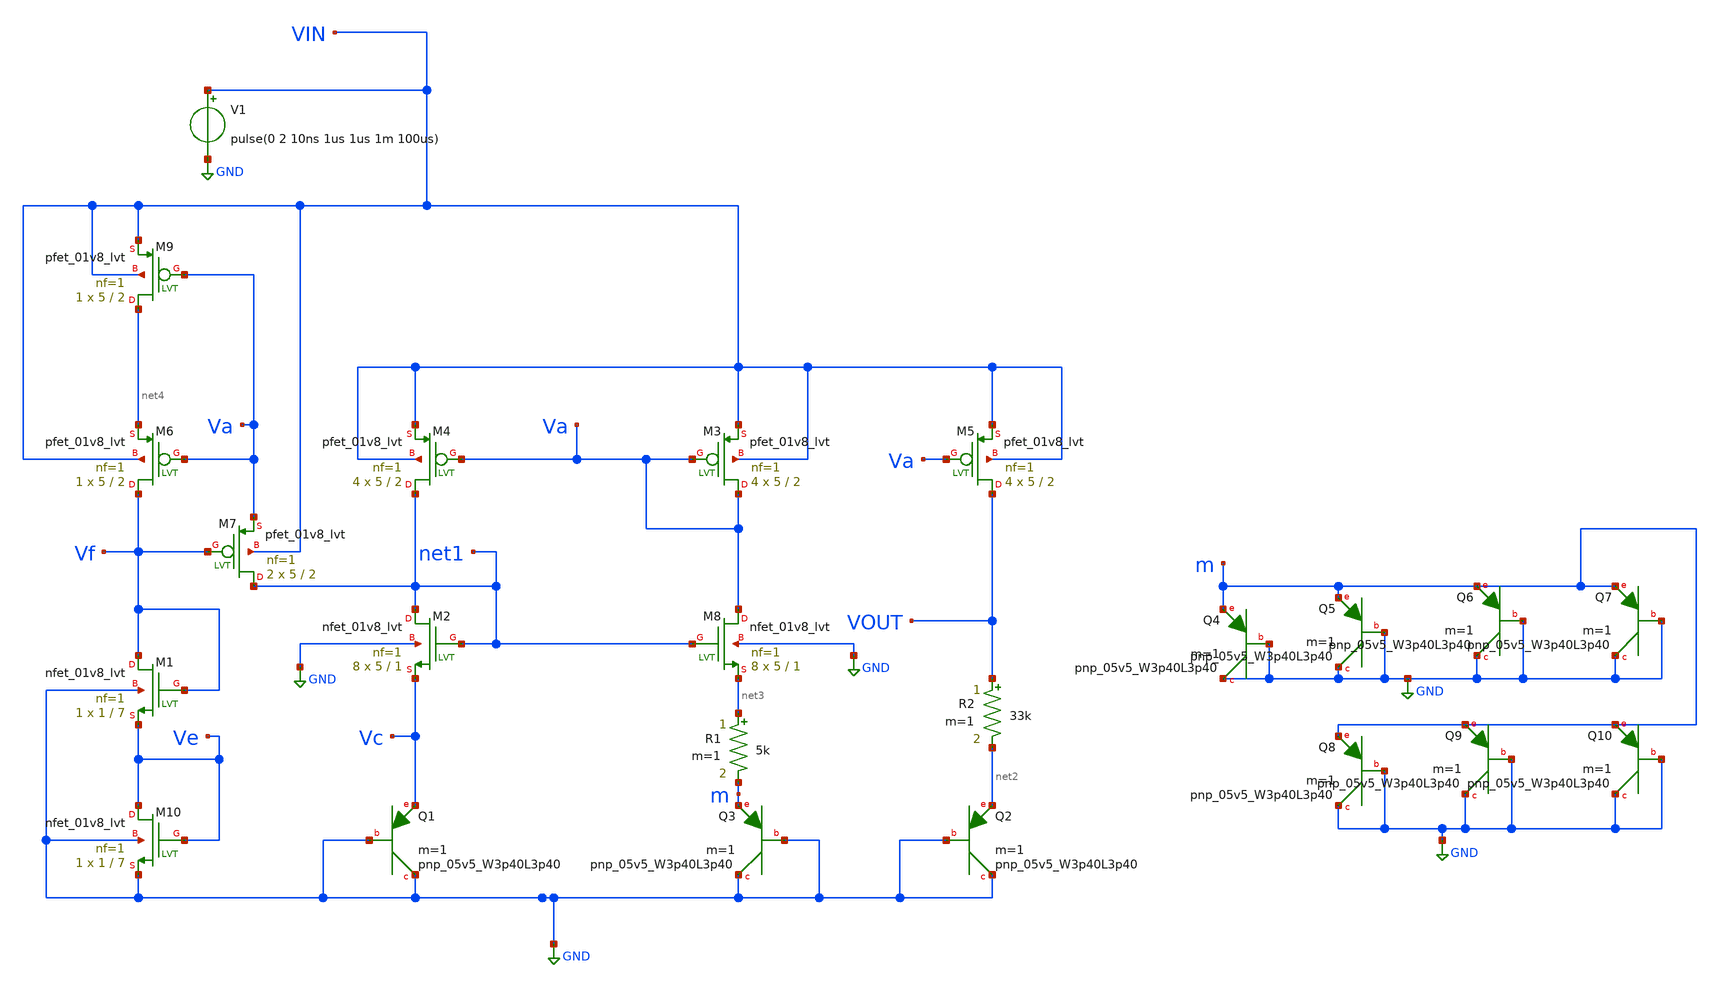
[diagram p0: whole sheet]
** sch_path: Bangap.sch
**.subckt Bangap
XM3 Va Va VIN VIN sky130_fd_pr__pfet_01v8_lvt L=2 W=5 nf=1 ad='int((nf+1)/2) * W/nf * 0.29' as='int((nf+2)/2) * W/nf * 0.29'
+ pd='2*int((nf+1)/2) * (W/nf + 0.29)' ps='2*int((nf+2)/2) * (W/nf + 0.29)' nrd='0.29 / W' nrs='0.29 / W'
+ sa=0 sb=0 sd=0 mult=4 m=4
XM4 net1 Va VIN VIN sky130_fd_pr__pfet_01v8_lvt L=2 W=5 nf=1 ad='int((nf+1)/2) * W/nf * 0.29' as='int((nf+2)/2) * W/nf * 0.29'
+ pd='2*int((nf+1)/2) * (W/nf + 0.29)' ps='2*int((nf+2)/2) * (W/nf + 0.29)' nrd='0.29 / W' nrs='0.29 / W'
+ sa=0 sb=0 sd=0 mult=4 m=4
XM5 VOUT Va VIN VIN sky130_fd_pr__pfet_01v8_lvt L=2 W=5 nf=1 ad='int((nf+1)/2) * W/nf * 0.29' as='int((nf+2)/2) * W/nf * 0.29'
+ pd='2*int((nf+1)/2) * (W/nf + 0.29)' ps='2*int((nf+2)/2) * (W/nf + 0.29)' nrd='0.29 / W' nrs='0.29 / W'
+ sa=0 sb=0 sd=0 mult=4 m=4
XM6 Vf Va net4 VIN sky130_fd_pr__pfet_01v8_lvt L=2 W=5 nf=1 ad='int((nf+1)/2) * W/nf * 0.29' as='int((nf+2)/2) * W/nf * 0.29'
+ pd='2*int((nf+1)/2) * (W/nf + 0.29)' ps='2*int((nf+2)/2) * (W/nf + 0.29)' nrd='0.29 / W' nrs='0.29 / W'
+ sa=0 sb=0 sd=0 mult=1 m=1
XM7 net1 Vf Va VIN sky130_fd_pr__pfet_01v8_lvt L=2 W=5 nf=1 ad='int((nf+1)/2) * W/nf * 0.29' as='int((nf+2)/2) * W/nf * 0.29'
+ pd='2*int((nf+1)/2) * (W/nf + 0.29)' ps='2*int((nf+2)/2) * (W/nf + 0.29)' nrd='0.29 / W' nrs='0.29 / W'
+ sa=0 sb=0 sd=0 mult=2 m=2
XQ1 GND GND Vc sky130_fd_pr__pnp_05v5_W3p40L3p40 m=1
XQ2 GND GND net2 sky130_fd_pr__pnp_05v5_W3p40L3p40 m=1
XQ3 GND GND m sky130_fd_pr__pnp_05v5_W3p40L3p40 m=1
R1 net3 m 5k m=1
R2 VOUT net2 33k m=1
V1 VIN GND pulse(0 2 10ns 1us 1us 1m 100us)
XM9 net4 Va VIN VIN sky130_fd_pr__pfet_01v8_lvt L=2 W=5 nf=1 ad='int((nf+1)/2) * W/nf * 0.29' as='int((nf+2)/2) * W/nf * 0.29'
+ pd='2*int((nf+1)/2) * (W/nf + 0.29)' ps='2*int((nf+2)/2) * (W/nf + 0.29)' nrd='0.29 / W' nrs='0.29 / W'
+ sa=0 sb=0 sd=0 mult=1 m=1
XM1 Vf Vf Ve GND sky130_fd_pr__nfet_01v8_lvt L=7 W=1 nf=1 ad='int((nf+1)/2) * W/nf * 0.29' as='int((nf+2)/2) * W/nf * 0.29'
+ pd='2*int((nf+1)/2) * (W/nf + 0.29)' ps='2*int((nf+2)/2) * (W/nf + 0.29)' nrd='0.29 / W' nrs='0.29 / W'
+ sa=0 sb=0 sd=0 mult=1 m=1
XM2 net1 net1 Vc GND sky130_fd_pr__nfet_01v8_lvt L=1 W=5 nf=1 ad='int((nf+1)/2) * W/nf * 0.29' as='int((nf+2)/2) * W/nf * 0.29'
+ pd='2*int((nf+1)/2) * (W/nf + 0.29)' ps='2*int((nf+2)/2) * (W/nf + 0.29)' nrd='0.29 / W' nrs='0.29 / W'
+ sa=0 sb=0 sd=0 mult=8 m=8
XM8 Va net1 net3 GND sky130_fd_pr__nfet_01v8_lvt L=1 W=5 nf=1 ad='int((nf+1)/2) * W/nf * 0.29' as='int((nf+2)/2) * W/nf * 0.29'
+ pd='2*int((nf+1)/2) * (W/nf + 0.29)' ps='2*int((nf+2)/2) * (W/nf + 0.29)' nrd='0.29 / W' nrs='0.29 / W'
+ sa=0 sb=0 sd=0 mult=8 m=8
XM10 Ve Ve GND GND sky130_fd_pr__nfet_01v8_lvt L=7 W=1 nf=1 ad='int((nf+1)/2) * W/nf * 0.29' as='int((nf+2)/2) * W/nf * 0.29'
+ pd='2*int((nf+1)/2) * (W/nf + 0.29)' ps='2*int((nf+2)/2) * (W/nf + 0.29)' nrd='0.29 / W' nrs='0.29 / W'
+ sa=0 sb=0 sd=0 mult=1 m=1
XQ4 GND GND m sky130_fd_pr__pnp_05v5_W3p40L3p40 m=1
XQ5 GND GND m sky130_fd_pr__pnp_05v5_W3p40L3p40 m=1
XQ6 GND GND m sky130_fd_pr__pnp_05v5_W3p40L3p40 m=1
XQ7 GND GND m sky130_fd_pr__pnp_05v5_W3p40L3p40 m=1
XQ8 GND GND m sky130_fd_pr__pnp_05v5_W3p40L3p40 m=1
XQ9 GND GND m sky130_fd_pr__pnp_05v5_W3p40L3p40 m=1
XQ10 GND GND m sky130_fd_pr__pnp_05v5_W3p40L3p40 m=1
**** begin user architecture code



.options TEMP = 27

* Models
.lib /usr/local/share/pdk/sky130A/libs.tech/ngspice/sky130.lib.spice tt
.iclude /usr/local/share/pdk/sky130A/libs.tech/ngspice/sky130_fd_pr__model__pnp.model.spice

* Data to save
.save all  @M.XM1.msky130_fd_pr__nfet_01v8_lvt[id]  @M.XM1.msky130_fd_pr__nfet_01v8_lvt[value]  @M.XM1.msky130_fd_pr__nfet_01v8_lvt[gm]  @M.XM1.msky130_fd_pr__nfet_01v8_lvt[vth]  @M.XM1.msky130_fd_pr__nfet_01v8_lvt[vds]  @M.XM1.msky130_fd_pr__nfet_01v8_lvt[vdsat]  @M.XM1.msky130_fd_pr__nfet_01v8_lvt[vgs]  @M.XM1.msky130_fd_pr__nfet_01v8_lvt[w]  @M.XM1.msky130_fd_pr__nfet_01v8_lvt[m]  @M.XM2.msky130_fd_pr__nfet_01v8_lvt[id]  @M.XM2.msky130_fd_pr__nfet_01v8_lvt[value]  @M.XM2.msky130_fd_pr__nfet_01v8_lvt[gm]  @M.XM2.msky130_fd_pr__nfet_01v8_lvt[vth]  @M.XM2.msky130_fd_pr__nfet_01v8_lvt[vds]  @M.XM2.msky130_fd_pr__nfet_01v8_lvt[vdsat]  @M.XM2.msky130_fd_pr__nfet_01v8_lvt[vgs]  @M.XM2.msky130_fd_pr__nfet_01v8_lvt[w]  @M.XM2.msky130_fd_pr__nfet_01v8_lvt[m]  @M.XM3.msky130_fd_pr__pfet_01v8_lvt[id]  @M.XM3.msky130_fd_pr__pfet_01v8_lvt[gm]  @M.XM3.msky130_fd_pr__pfet_01v8_lvt[vth]  @M.XM3.msky130_fd_pr__pfet_01v8_lvt[vsd]  @M.XM3.msky130_fd_pr__pfet_01v8_lvt[vdsat]  @M.XM3.msky130_fd_pr__pfet_01v8_lvt[vsg]  @M.XM3.msky130_fd_pr__pfet_01v8_lvt[w]  @M.XM3.msky130_fd_pr__pfet_01v8_lvt[m]  @M.XM4.msky130_fd_pr__pfet_01v8_lvt[id]  @M.XM4.msky130_fd_pr__pfet_01v8_lvt[gm]  @M.XM4.msky130_fd_pr__pfet_01v8_lvt[vth]  @M.XM4.msky130_fd_pr__pfet_01v8_lvt[vsd]  @M.XM4.msky130_fd_pr__pfet_01v8_lvt[vdsat]  @M.XM4.msky130_fd_pr__pfet_01v8_lvt[vsg]  @M.XM4.msky130_fd_pr__pfet_01v8_lvt[w]  @M.XM4.msky130_fd_pr__pfet_01v8_lvt[m]  @M.XM5.msky130_fd_pr__pfet_01v8_lvt[id]  @M.XM5.msky130_fd_pr__pfet_01v8_lvt[gm]  @M.XM5.msky130_fd_pr__pfet_01v8_lvt[vth]  @M.XM5.msky130_fd_pr__pfet_01v8_lvt[vsd]  @M.XM5.msky130_fd_pr__pfet_01v8_lvt[vdsat]  @M.XM5.msky130_fd_pr__pfet_01v8_lvt[vsg]  @M.XM5.msky130_fd_pr__pfet_01v8_lvt[w]  @M.XM5.msky130_fd_pr__pfet_01v8_lvt[m]  @M.XM6.msky130_fd_pr__pfet_01v8_lvt[id]  @M.XM6.msky130_fd_pr__pfet_01v8_lvt[gm]  @M.XM6.msky130_fd_pr__pfet_01v8_lvt[vth]  @M.XM6.msky130_fd_pr__pfet_01v8_lvt[vsd]  @M.XM6.msky130_fd_pr__pfet_01v8_lvt[vdsat]  @M.XM6.msky130_fd_pr__pfet_01v8_lvt[vsg]  @M.XM6.msky130_fd_pr__pfet_01v8_lvt[w]  @M.XM6.msky130_fd_pr__pfet_01v8_lvt[m]  @M.XM7.msky130_fd_pr__pfet_01v8_lvt[id]  @M.XM7.msky130_fd_pr__pfet_01v8_lvt[gm]  @M.XM7.msky130_fd_pr__pfet_01v8_lvt[vth]  @M.XM7.msky130_fd_pr__pfet_01v8_lvt[vsd]  @M.XM7.msky130_fd_pr__pfet_01v8_lvt[vdsat]  @M.XM7.msky130_fd_pr__pfet_01v8_lvt[vsg]  @M.XM7.msky130_fd_pr__pfet_01v8_lvt[w]  @M.XM7.msky130_fd_pr__pfet_01v8_lvt[m]  @M.XM8.msky130_fd_pr__nfet_01v8_lvt[id]  @M.XM8.msky130_fd_pr__nfet_01v8_lvt[value]  @M.XM8.msky130_fd_pr__nfet_01v8_lvt[gm]  @M.XM8.msky130_fd_pr__nfet_01v8_lvt[vth]  @M.XM8.msky130_fd_pr__nfet_01v8_lvt[vds]  @M.XM8.msky130_fd_pr__nfet_01v8_lvt[vdsat]  @M.XM8.msky130_fd_pr__nfet_01v8_lvt[vgs]  @M.XM8.msky130_fd_pr__nfet_01v8_lvt[w]  @M.XM8.msky130_fd_pr__nfet_01v8_lvt[m]  @M.XM9.msky130_fd_pr__pfet_01v8_lvt[id]  @M.XM9.msky130_fd_pr__pfet_01v8_lvt[gm]  @M.XM9.msky130_fd_pr__pfet_01v8_lvt[vth]  @M.XM9.msky130_fd_pr__pfet_01v8_lvt[vsd]  @M.XM9.msky130_fd_pr__pfet_01v8_lvt[vdsat]  @M.XM9.msky130_fd_pr__pfet_01v8_lvt[vsg]  @M.XM9.msky130_fd_pr__pfet_01v8_lvt[w]  @M.XM9.msky130_fd_pr__pfet_01v8_lvt[m]  @M.XM10.msky130_fd_pr__nfet_01v8_lvt[id]  @M.XM10.msky130_fd_pr__nfet_01v8_lvt[value]  @M.XM10.msky130_fd_pr__nfet_01v8_lvt[gm]  @M.XM10.msky130_fd_pr__nfet_01v8_lvt[vth]  @M.XM10.msky130_fd_pr__nfet_01v8_lvt[vds]  @M.XM10.msky130_fd_pr__nfet_01v8_lvt[vdsat]  @M.XM10.msky130_fd_pr__nfet_01v8_lvt[vgs]  @M.XM10.msky130_fd_pr__nfet_01v8_lvt[w]  @M.XM10.msky130_fd_pr__nfet_01v8_lvt[m]  @M.XQ1.msky130_fd_pr__pnp_05v5_W3p40L3p40[e]  @M.XQ1.msky130_fd_pr__pnp_05v5_W3p40L3p40[b]  @M.XQ1.msky130_fd_pr__pnp_05v5_W3p40L3p40[c]  @M.XQ2.msky130_fd_pr__pnp_05v5_W3p40L3p40[e]  @M.XQ2.msky130_fd_pr__pnp_05v5_W3p40L3p40[b]  @M.XQ2.msky130_fd_pr__pnp_05v5_W3p40L3p40[c]  @M.XQ3.msky130_fd_pr__pnp_05v5_W3p40L3p40[e]  @M.XQ3.msky130_fd_pr__pnp_05v5_W3p40L3p40[b]  @M.XQ3.msky130_fd_pr__pnp_05v5_W3p40L3p40[c]

* Simulation
.control

tran 5n 10u
let gm_id2=@M.XM4.msky130_fd_pr__pfet_01v8_lvt[gm]/@M.XM4.msky130_fd_pr__pfet_01v8_lvt[id]
plot @M.XM9.msky130_fd_pr__pfet_01v8_lvt[id] @M.XM6.msky130_fd_pr__pfet_01v8_lvt[id]
+ @M.XM1.msky130_fd_pr__nfet_01v8_lvt[id] @M.XM10.msky130_fd_pr__nfet_01v8_lvt[id] @M.XM7.msky130_fd_pr__pfet_01v8_lvt[id]
plot @M.XM4.msky130_fd_pr__pfet_01v8_lvt[id] @M.XM2.msky130_fd_pr__nfet_01v8_lvt[id]
plot @M.XM3.msky130_fd_pr__pfet_01v8_lvt[id] @M.XM8.msky130_fd_pr__nfet_01v8_lvt[id]
plot @M.XM5.msky130_fd_pr__pfet_01v8_lvt[id]


.endc
.end


**** end user architecture code
**.ends
.GLOBAL GND
.end
